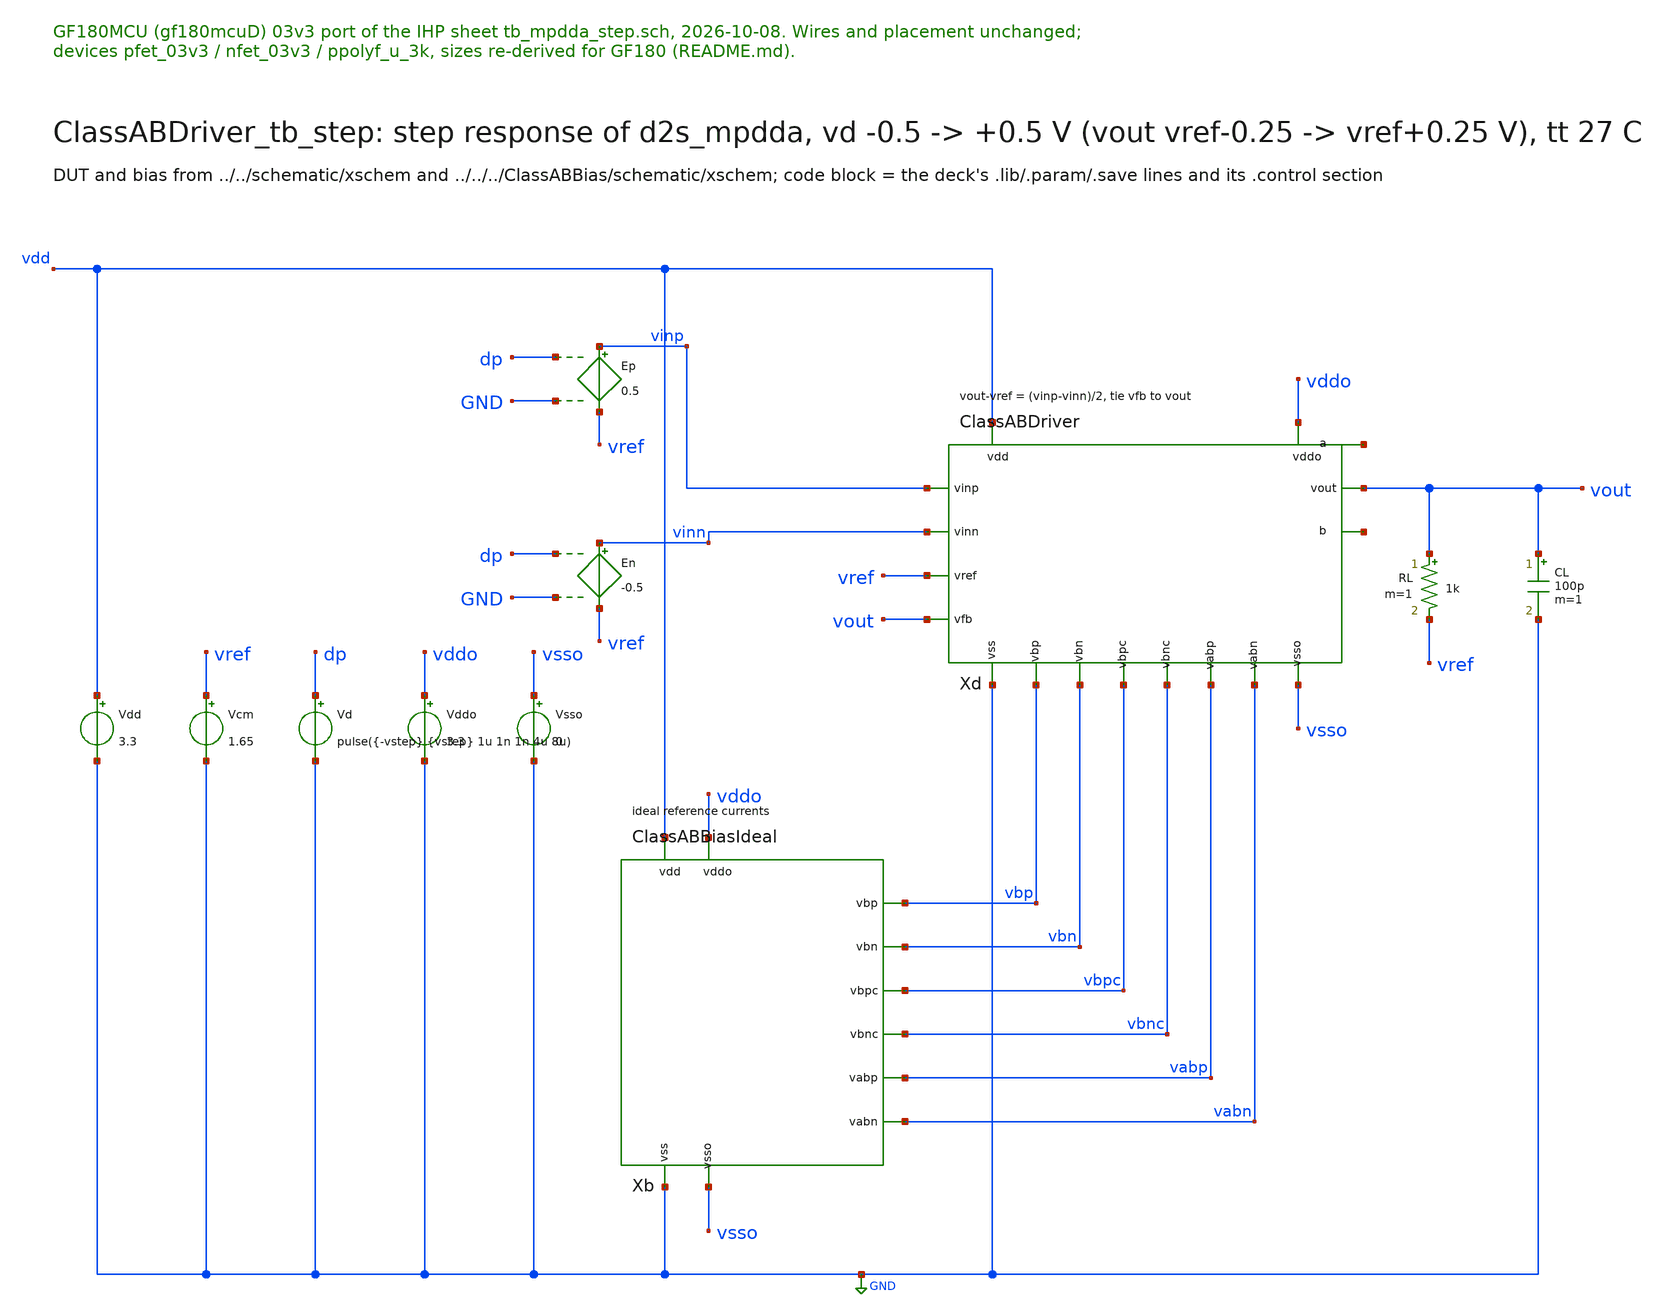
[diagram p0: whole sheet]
** sch_path: macros/ClassABDriver/testbenches/xschem/ClassABDriver_tb_step.sch
**.subckt ClassABDriver_tb_step
Vdd vdd GND 3.3
Vcm vref GND 1.65
Xb vdd GND vddo vsso vbp vbn vbpc vbnc vabp vabn ClassABBiasIdeal
Xd vdd GND vddo vsso vinp vinn vref vout vout vbp vbn vbpc vbnc vabp vabn net1 net2 ClassABDriver
Vd dp GND pulse({-vstep} {vstep} 1u 1n 1n 4u 8u)
Ep vinp vref dp GND 0.5
En vinn vref dp GND -0.5
RL vout vref 1k m=1
CL vout GND 100p m=1
Vddo vddo GND 3.3
Vsso vsso GND 0
**** begin user architecture code

.param vstep=0.5
.control
tran 2n 9u
meas tran vlo find v(vout) at=0.99u
meas tran vhi find v(vout) at=4.9u
meas tran vmax max v(vout) from=1u to=5u
let os = 100*(vmax - vhi)/(vhi - vlo)
let v10 = vlo + 0.1*(vhi - vlo)
let v90 = vlo + 0.9*(vhi - vlo)
meas tran t10 when v(vout)=v10 rise=1
meas tran t90 when v(vout)=v90 rise=1
let rate = 0.8*(vhi - vlo)/(t90 - t10)
print vlo vhi os rate
if $?batchmode = 0
  plot v(vout) v(vinp) v(vinn)
end
.endc


.include $::180MCU_MODELS/design.ngspice
.lib $::180MCU_MODELS/sm141064.ngspice typical
.lib $::180MCU_MODELS/sm141064.ngspice res_typical
.lib $::180MCU_MODELS/sm141064.ngspice moscap_typical

**** end user architecture code
**.ends
.GLOBAL GND
.end
